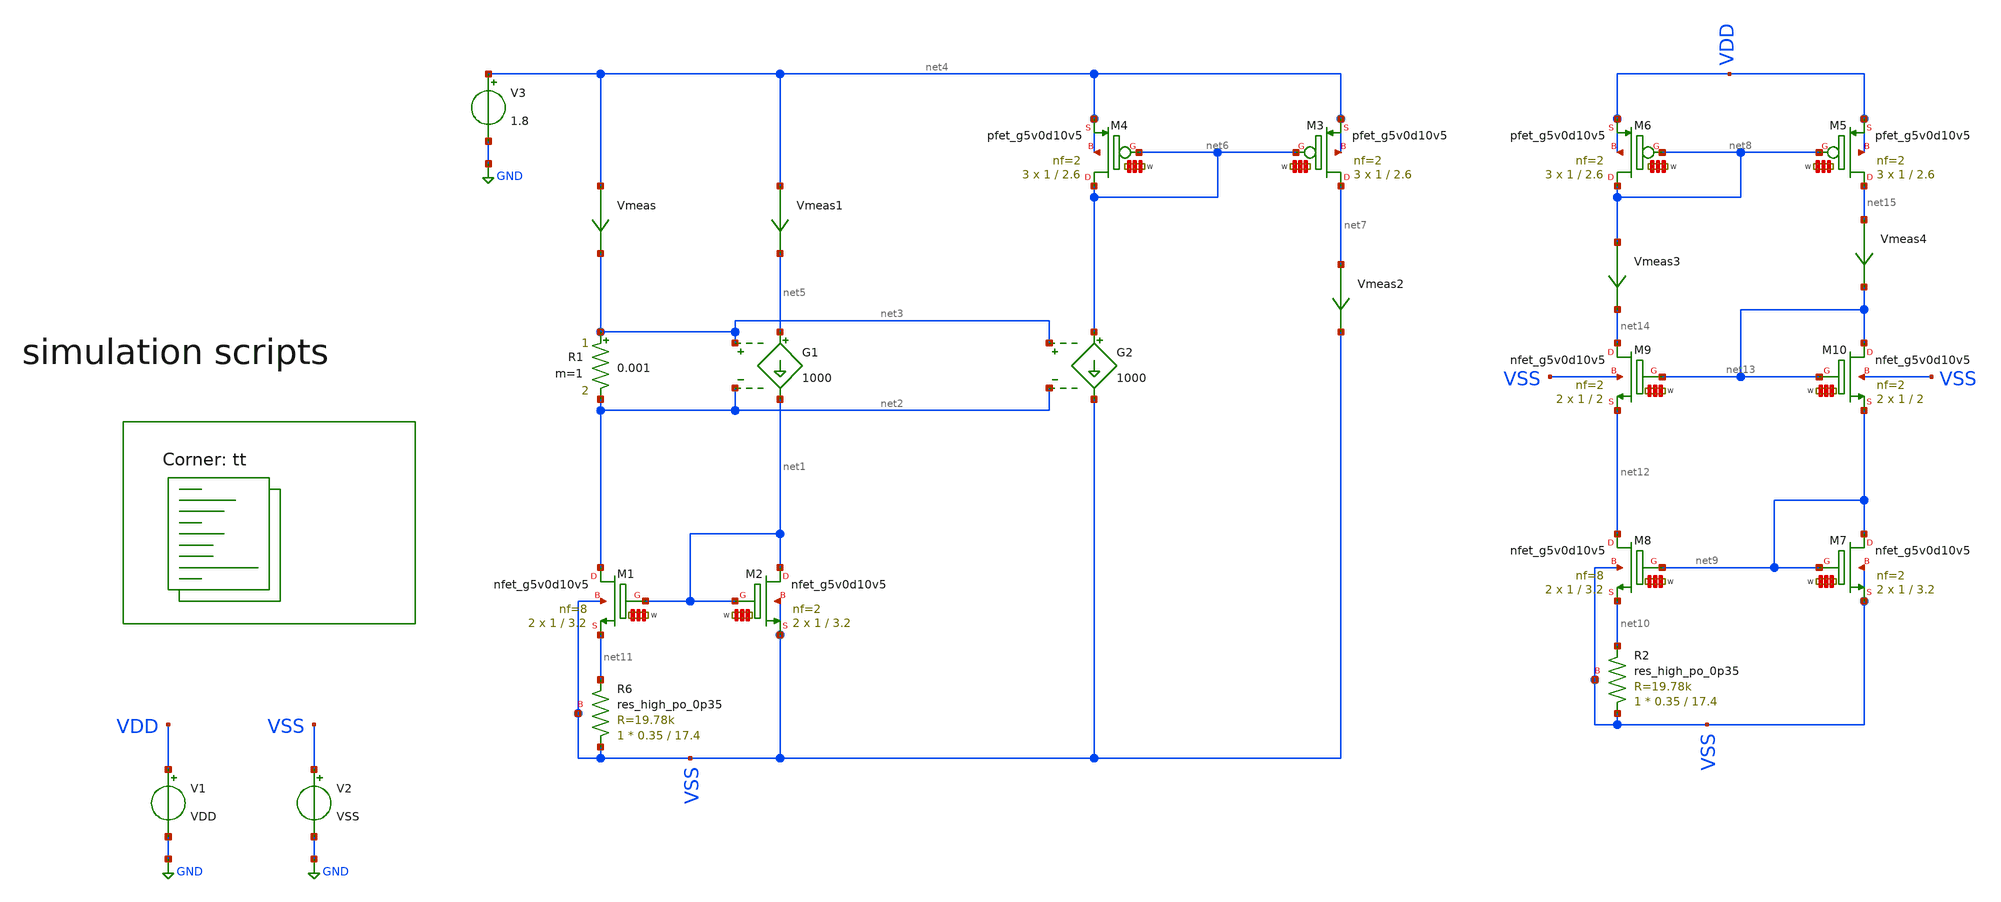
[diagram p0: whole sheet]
** sch_path: Learning/single_ended_amplifiers/Design_and_Analysis_of_Two-Stage_CMOS_Operational_Amplifier_for_Fluorescence_Signal_Processing_sky130_5V/transimpedance_cell_design/transcondutance_cell_design.sch
**.subckt transcondutance_cell_design
V1 VDD GND VDD
V2 VSS GND VSS
XR6 VSS net11 VSS sky130_fd_pr__res_high_po_0p35 L=17.4 mult=1 m=1
R1 net3 net2 0.001 m=1
G1 net5 net1 net3 net2 1000
Vmeas net4 net3 0
.save i(vmeas)
Vmeas1 net4 net5 0
.save i(vmeas1)
V3 net4 GND 1.8
XM1 net2 net1 net11 VSS sky130_fd_pr__nfet_g5v0d10v5 L=3.2 W='1 * 8 ' nf=8 ad='int((nf+1)/2) * W / nf * 0.29'
+ as='int((nf+2)/2) * W / nf * 0.29' pd='2*int((nf+1)/2) * (W / nf + 0.29)' ps='2*int((nf+2)/2) * (W / nf + 0.29)'
+ nrd='0.29 / W ' nrs='0.29 / W ' sa=0 sb=0 sd=0 mult=2 m=2
XM2 net1 net1 VSS VSS sky130_fd_pr__nfet_g5v0d10v5 L=3.2 W='1 * 2 ' nf=2 ad='int((nf+1)/2) * W / nf * 0.29'
+ as='int((nf+2)/2) * W / nf * 0.29' pd='2*int((nf+1)/2) * (W / nf + 0.29)' ps='2*int((nf+2)/2) * (W / nf + 0.29)'
+ nrd='0.29 / W ' nrs='0.29 / W ' sa=0 sb=0 sd=0 mult=2 m=2
G2 net6 VSS net3 net2 1000
XM4 net6 net6 net4 net4 sky130_fd_pr__pfet_g5v0d10v5 L=2.6 W='1 * 2 ' nf=2 ad='int((2 + 1)/2) * 1 * 0.29'
+ as='int((2 + 2)/2) * 1 * 0.29' pd='2*int((2 + 1)/2) * (1 + 0.29)' ps='2*int((2 + 2)/2) * (1 + 0.29)'
+ nrd='0.29 / 1 / 2 ' nrs='0.29 / 1 / 2 ' sa=0 sb=0 sd=0 mult=3 m=3
XM3 net7 net6 net4 net4 sky130_fd_pr__pfet_g5v0d10v5 L=2.6 W='1 * 2 ' nf=2 ad='int((2 + 1)/2) * 1 * 0.29'
+ as='int((2 + 2)/2) * 1 * 0.29' pd='2*int((2 + 1)/2) * (1 + 0.29)' ps='2*int((2 + 2)/2) * (1 + 0.29)'
+ nrd='0.29 / 1 / 2 ' nrs='0.29 / 1 / 2 ' sa=0 sb=0 sd=0 mult=3 m=3
Vmeas2 net7 VSS 0
.save i(vmeas2)
Vmeas3 net8 net14 0
.save i(vmeas3)
Vmeas4 net15 net13 0
.save i(vmeas4)
XM5 net15 net8 VDD VDD sky130_fd_pr__pfet_g5v0d10v5 L=2.6 W='1 * 2 ' nf=2 ad='int((2 + 1)/2) * 1 * 0.29'
+ as='int((2 + 2)/2) * 1 * 0.29' pd='2*int((2 + 1)/2) * (1 + 0.29)' ps='2*int((2 + 2)/2) * (1 + 0.29)'
+ nrd='0.29 / 1 / 2 ' nrs='0.29 / 1 / 2 ' sa=0 sb=0 sd=0 mult=3 m=3
XM6 net8 net8 VDD VDD sky130_fd_pr__pfet_g5v0d10v5 L=2.6 W='1 * 2 ' nf=2 ad='int((2 + 1)/2) * 1 * 0.29'
+ as='int((2 + 2)/2) * 1 * 0.29' pd='2*int((2 + 1)/2) * (1 + 0.29)' ps='2*int((2 + 2)/2) * (1 + 0.29)'
+ nrd='0.29 / 1 / 2 ' nrs='0.29 / 1 / 2 ' sa=0 sb=0 sd=0 mult=3 m=3
XR2 VSS net10 VSS sky130_fd_pr__res_high_po_0p35 L=17.4 mult=1 m=1
XM7 net9 net9 VSS VSS sky130_fd_pr__nfet_g5v0d10v5 L=3.2 W='1 * 2 ' nf=2 ad='int((nf+1)/2) * W / nf * 0.29'
+ as='int((nf+2)/2) * W / nf * 0.29' pd='2*int((nf+1)/2) * (W / nf + 0.29)' ps='2*int((nf+2)/2) * (W / nf + 0.29)'
+ nrd='0.29 / W ' nrs='0.29 / W ' sa=0 sb=0 sd=0 mult=2 m=2
XM8 net12 net9 net10 VSS sky130_fd_pr__nfet_g5v0d10v5 L=3.2 W='1 * 8 ' nf=8 ad='int((nf+1)/2) * W / nf * 0.29'
+ as='int((nf+2)/2) * W / nf * 0.29' pd='2*int((nf+1)/2) * (W / nf + 0.29)' ps='2*int((nf+2)/2) * (W / nf + 0.29)'
+ nrd='0.29 / W ' nrs='0.29 / W ' sa=0 sb=0 sd=0 mult=2 m=2
XM9 net14 net13 net12 VSS sky130_fd_pr__nfet_g5v0d10v5 L=2 W='1 * 2 ' nf=2 ad='int((nf+1)/2) * W / nf * 0.29'
+ as='int((nf+2)/2) * W / nf * 0.29' pd='2*int((nf+1)/2) * (W / nf + 0.29)' ps='2*int((nf+2)/2) * (W / nf + 0.29)'
+ nrd='0.29 / W ' nrs='0.29 / W ' sa=0 sb=0 sd=0 mult=2 m=2
XM10 net13 net13 net9 VSS sky130_fd_pr__nfet_g5v0d10v5 L=2 W='1 * 2 ' nf=2 ad='int((nf+1)/2) * W / nf * 0.29'
+ as='int((nf+2)/2) * W / nf * 0.29' pd='2*int((nf+1)/2) * (W / nf + 0.29)' ps='2*int((nf+2)/2) * (W / nf + 0.29)'
+ nrd='0.29 / W ' nrs='0.29 / W ' sa=0 sb=0 sd=0 mult=2 m=2
**** begin user architecture code
.lib $::SKYWATER_MODELS/sky130.lib.spice tt


.Temp 27
.param VDD = 5
.param VSS = 0


.control
save all

save @m.xm2.msky130_fd_pr__nfet_g5v0d10v5[vdsat]

dc Temp -40 125 1
plot i(Vmeas1) i(Vmeas2)
plot i(Vmeas3) i(Vmeas4)
wrdata data.csv i(Vmeas3) i(Vmeas4)


op
print i(Vmeas1)
print v(net2)




.endc

**** end user architecture code
**.ends
.GLOBAL GND
.end
